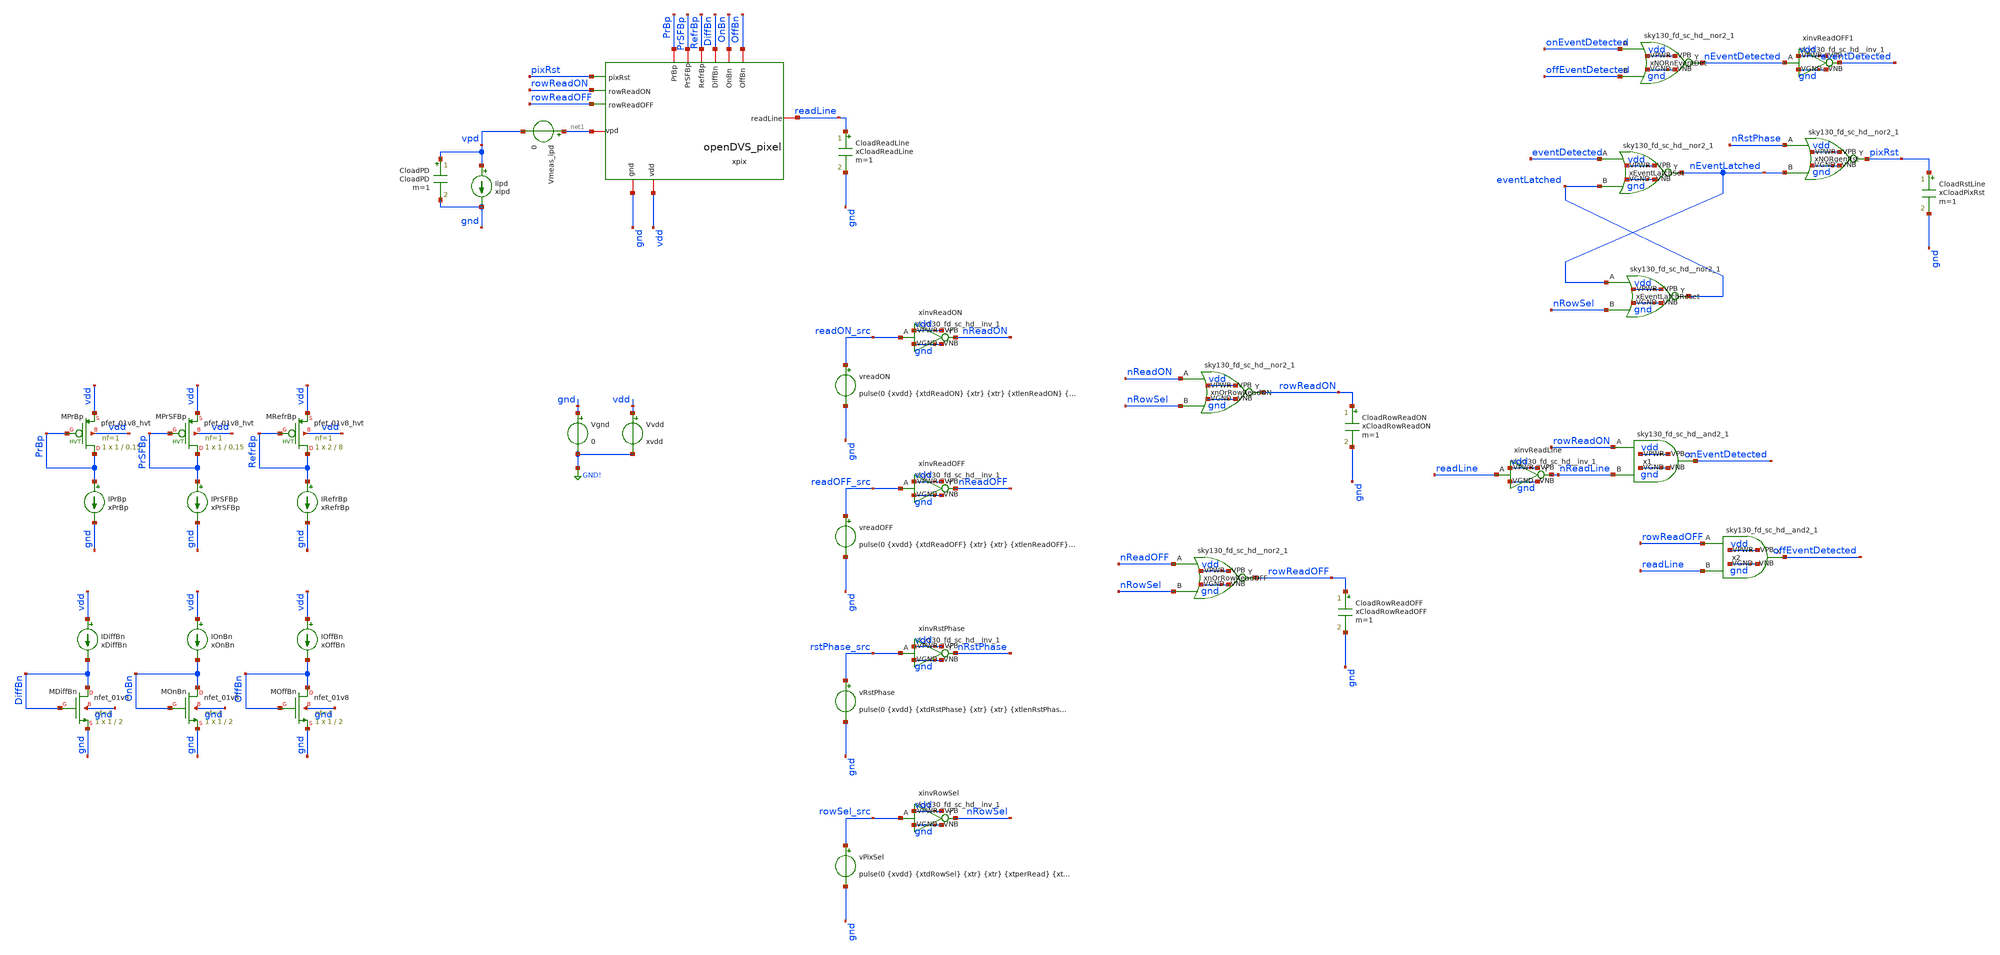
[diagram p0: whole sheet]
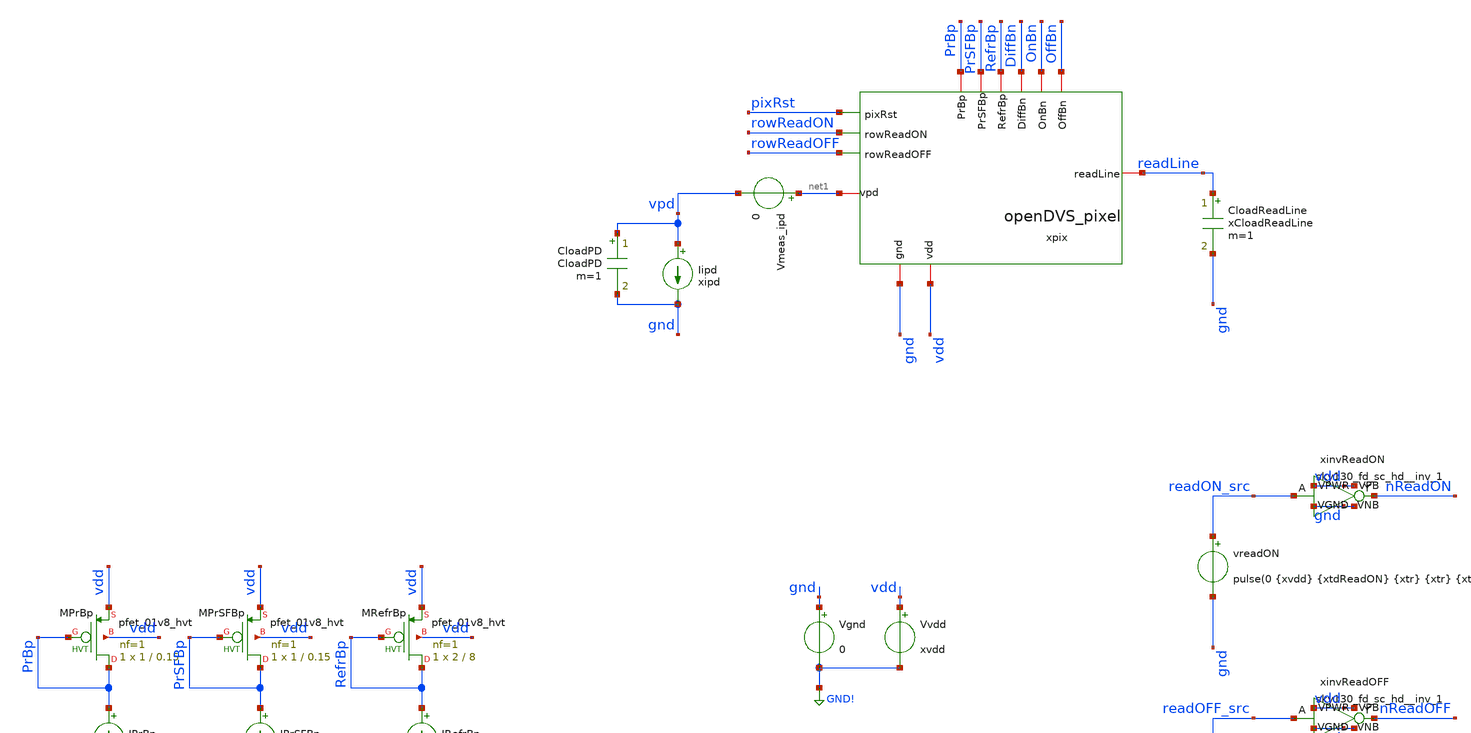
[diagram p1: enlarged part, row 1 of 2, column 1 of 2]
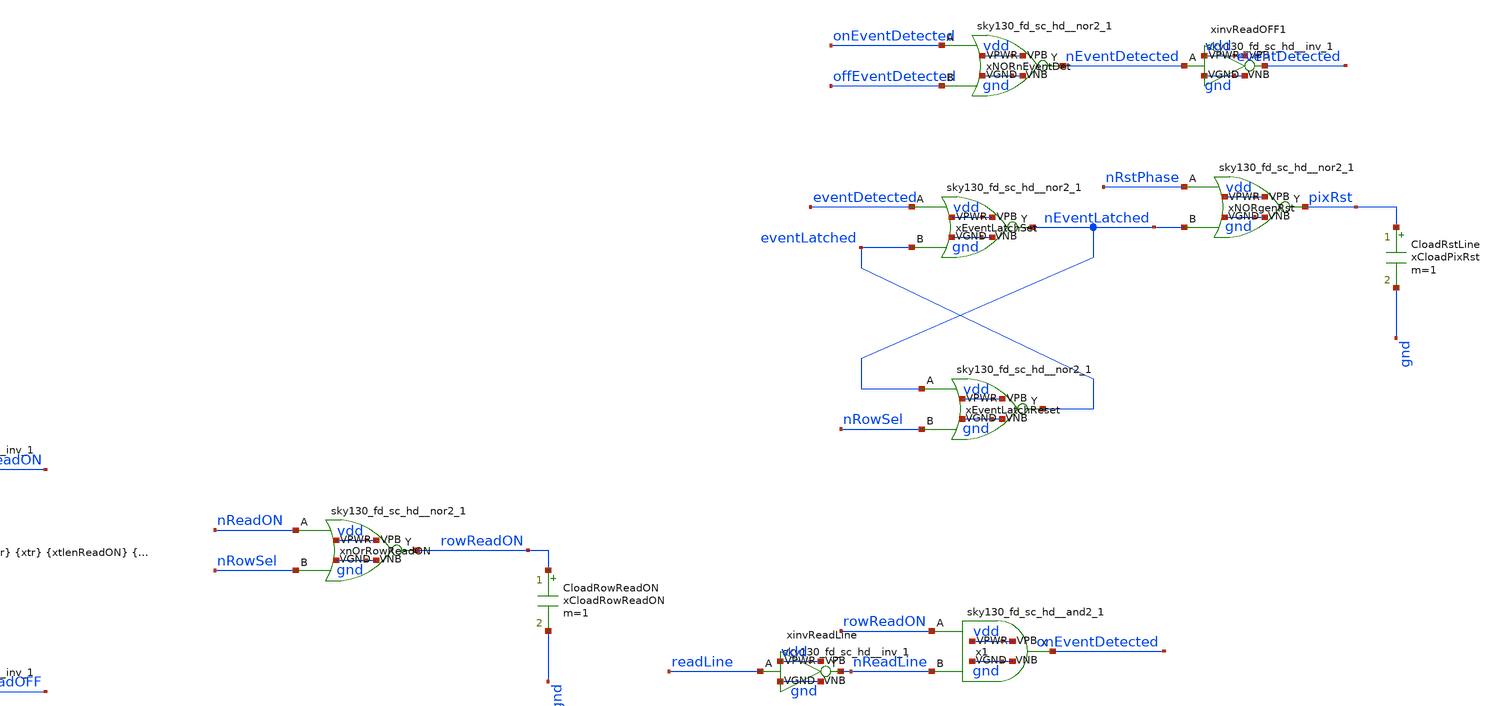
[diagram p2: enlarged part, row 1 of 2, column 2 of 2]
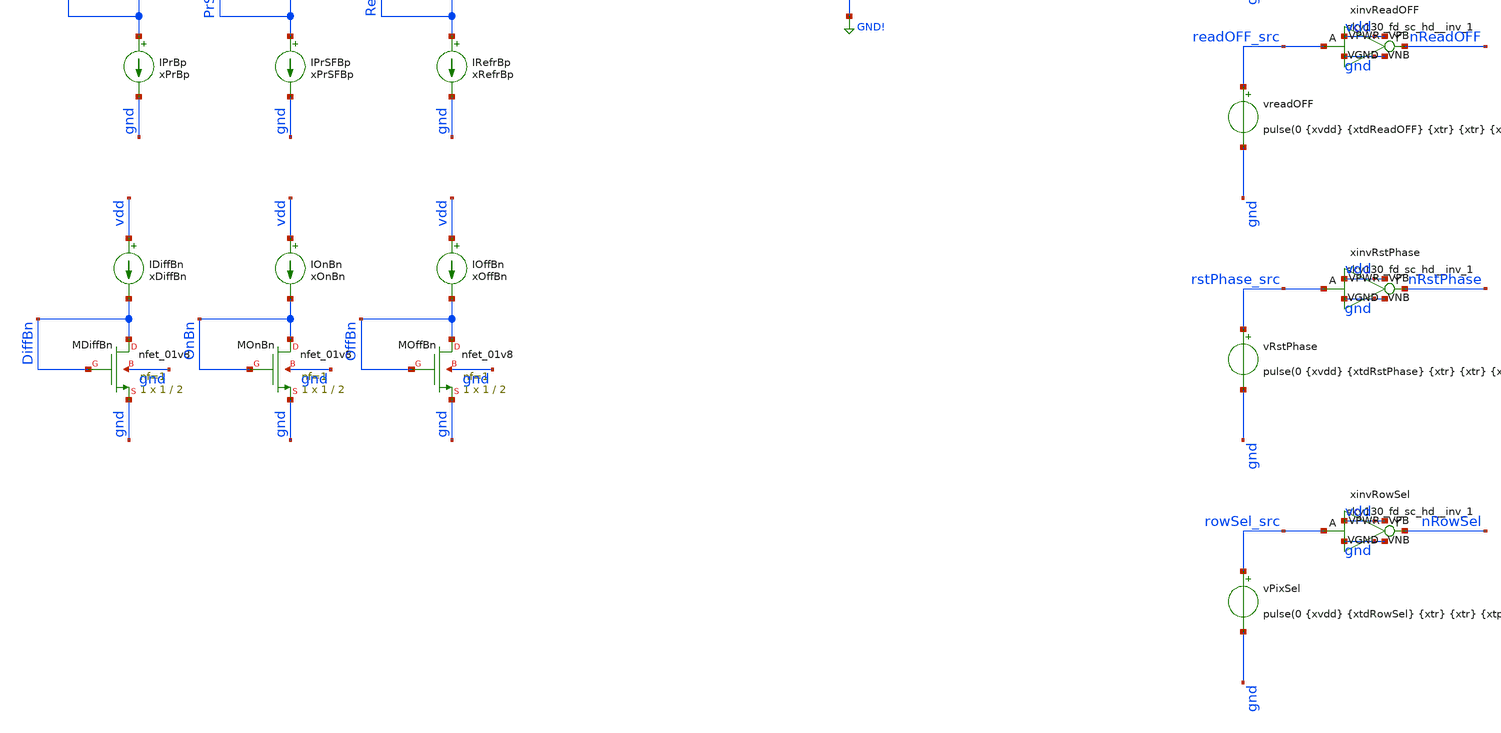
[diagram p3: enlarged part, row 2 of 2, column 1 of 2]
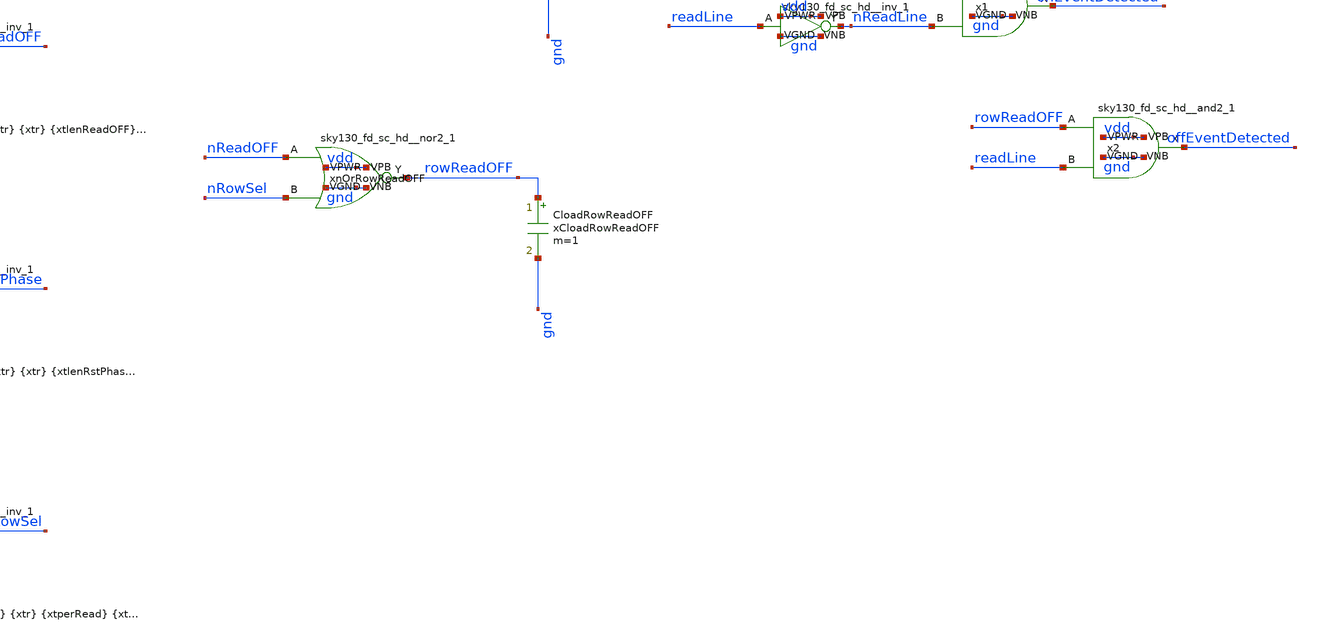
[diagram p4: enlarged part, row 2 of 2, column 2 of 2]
** sch_path: analog/xschem/pixel_tb.sch
**.subckt pixel_tb
xpix rowReadON vdd PrBp gnd net1 rowReadOFF pixRst PrSFBp DiffBn OnBn OffBn RefrBp readLine
+ openDVS_pixel
Vgnd gnd GND! 0
Vvdd vdd GND! xvdd
Iipd vpd gnd xipd
IRefrBp RefrBp gnd xRefrBp
XMRefrBp RefrBp RefrBp vdd vdd sky130_fd_pr__pfet_01v8_hvt L=8 W=2 nf=1 ad='int((1 + 1)/2) * 2 / 1 * 0.29'
+ as='int((1 + 2)/2) * 2 / 1 * 0.29' pd='2*int((1 + 1)/2) * (2 / 1 + 0.29)' ps='2*int((1 + 2)/2) * (2 / 1 + 0.29)'
+ nrd='0.29 / 2 ' nrs='0.29 / 2 ' sa=0 sb=0 sd=0 mult=1 m=1
IPrBp PrBp gnd xPrBp
XMPrBp PrBp PrBp vdd vdd sky130_fd_pr__pfet_01v8_hvt L=0.15 W=1 nf=1 ad='int((1 + 1)/2) * 1 / 1 * 0.29'
+ as='int((1 + 2)/2) * 1 / 1 * 0.29' pd='2*int((1 + 1)/2) * (1 / 1 + 0.29)' ps='2*int((1 + 2)/2) * (1 / 1 + 0.29)'
+ nrd='0.29 / 1 ' nrs='0.29 / 1 ' sa=0 sb=0 sd=0 mult=1 m=1
IPrSFBp PrSFBp gnd xPrSFBp
XMPrSFBp PrSFBp PrSFBp vdd vdd sky130_fd_pr__pfet_01v8_hvt L=0.15 W=1 nf=1 ad='int((1 + 1)/2) * 1 / 1 * 0.29'
+ as='int((1 + 2)/2) * 1 / 1 * 0.29' pd='2*int((1 + 1)/2) * (1 / 1 + 0.29)' ps='2*int((1 + 2)/2) * (1 / 1 + 0.29)'
+ nrd='0.29 / 1 ' nrs='0.29 / 1 ' sa=0 sb=0 sd=0 mult=1 m=1
XMDiffBn DiffBn DiffBn gnd gnd sky130_fd_pr__nfet_01v8 L=2 W=1 nf=1 ad='int((1 + 1)/2) * 1 / 1 * 0.29'
+ as='int((1 + 2)/2) * 1 / 1 * 0.29' pd='2*int((1 + 1)/2) * (1 / 1 + 0.29)' ps='2*int((1 + 2)/2) * (1 / 1 + 0.29)'
+ nrd='0.29 / 1 ' nrs='0.29 / 1 ' sa=0 sb=0 sd=0 mult=1 m=1
IDiffBn vdd DiffBn xDiffBn
XMOnBn OnBn OnBn gnd gnd sky130_fd_pr__nfet_01v8 L=2 W=1 nf=1 ad='int((1 + 1)/2) * 1 / 1 * 0.29' as='int((1 + 2)/2) * 1 / 1 * 0.29'
+ pd='2*int((1 + 1)/2) * (1 / 1 + 0.29)' ps='2*int((1 + 2)/2) * (1 / 1 + 0.29)' nrd='0.29 / 1 ' nrs='0.29 / 1 '
+ sa=0 sb=0 sd=0 mult=1 m=1
IOnBn vdd OnBn xOnBn
XMOffBn OffBn OffBn gnd gnd sky130_fd_pr__nfet_01v8 L=2 W=1 nf=1 ad='int((1 + 1)/2) * 1 / 1 * 0.29' as='int((1 + 2)/2) * 1 / 1 * 0.29'
+ pd='2*int((1 + 1)/2) * (1 / 1 + 0.29)' ps='2*int((1 + 2)/2) * (1 / 1 + 0.29)' nrd='0.29 / 1 ' nrs='0.29 / 1 '
+ sa=0 sb=0 sd=0 mult=1 m=1
IOffBn vdd OffBn xOffBn
vreadON readON_src gnd pulse(0 {xvdd} {xtdReadON} {xtr} {xtr} {xtlenReadON} {xtperRead})
CloadRowReadOFF rowReadOFF gnd xCloadRowReadOFF m=1
vreadOFF readOFF_src gnd pulse(0 {xvdd} {xtdReadOFF} {xtr} {xtr} {xtlenReadOFF} {xtperRead})
vPixSel rowSel_src gnd pulse(0 {xvdd} {xtdRowSel} {xtr} {xtr} {xtperRead} {xtperRowSel})
CloadReadLine readLine gnd xCloadReadLine m=1
xinvReadON readON_src nReadON vdd vdd gnd gnd sky130_fd_sc_hd__inv_1
xinvReadOFF readOFF_src nReadOFF vdd vdd gnd gnd sky130_fd_sc_hd__inv_1
xinvRowSel rowSel_src nRowSel vdd vdd gnd gnd sky130_fd_sc_hd__inv_1
xnOrRowReadOFF nReadOFF nRowSel rowReadOFF vdd vdd gnd gnd sky130_fd_sc_hd__nor2_1
CloadRowReadON rowReadON gnd xCloadRowReadON m=1
xnOrRowReadON nReadON nRowSel rowReadON vdd vdd gnd gnd sky130_fd_sc_hd__nor2_1
x1 rowReadON nReadLine vdd vdd gnd gnd onEventDetected sky130_fd_sc_hd__and2_1
xinvReadLine readLine nReadLine vdd vdd gnd gnd sky130_fd_sc_hd__inv_1
x2 rowReadOFF readLine vdd vdd gnd gnd offEventDetected sky130_fd_sc_hd__and2_1
xNORnEventDet onEventDetected offEventDetected nEventDetected vdd vdd gnd gnd
+ sky130_fd_sc_hd__nor2_1
xinvReadOFF1 nEventDetected eventDetected vdd vdd gnd gnd sky130_fd_sc_hd__inv_1
xEventLatchSet eventDetected eventLatched nEventLatched vdd vdd gnd gnd sky130_fd_sc_hd__nor2_1
xEventLatchReset nEventLatched nRowSel eventLatched vdd vdd gnd gnd sky130_fd_sc_hd__nor2_1
vRstPhase rstPhase_src gnd pulse(0 {xvdd} {xtdRstPhase} {xtr} {xtr} {xtlenRstPhase} {xtperRowSel})
xinvRstPhase rstPhase_src nRstPhase vdd vdd gnd gnd sky130_fd_sc_hd__inv_1
xNORgenRst nRstPhase nEventLatched pixRst vdd vdd gnd gnd sky130_fd_sc_hd__nor2_1
CloadRstLine pixRst gnd xCloadPixRst m=1
CloadPD vpd gnd CloadPD m=1
Vmeas_ipd net1 vpd 0
**** begin user architecture code

** opencircuitdesign pdks install
.lib $::SKYWATER_MODELS/sky130.lib.spice tt




.param xvdd = 1.8
.param xipd = 1e-9
.param xPrBp = 10n
.param xPrSFBp = 1n
.param xRefrBp = 4u
.param xDiffBn = 10n
.param xOnBn = 100n
.param xOffBn = 1n

.param xtr = 0.1n
.param xtperRead = 3u
.param xtdReadON = 100n
.param xtlenReadON = 950n
.param xtlenReadOFF = 950n
.param xtlenRstPhase = 950n
.param xtdReadOFF = 'xtdReadON+xtlenReadON+10n'
.param xtdRstPhase = 'xtdReadOFF+xtlenReadOFF+10n'
.param xtdRowSel = 50n
.param xtperRowSel = '2*xtperRead'

.param CloadPD = 30f
.param xCloadReadLine = 300f
.param xCloadRowReadON = 300f
.param xCloadRowReadOFF = 300f
.param xCloadPixRst = 300f

*Small Iphoto testing
Iphoto1 vpd gnd pulse(50n 100n 12u 5n 5n 5.99u 30u)
Iphoto2 vpd gnd pulse(50n 25n 24u 5n 5n 5.99u 30u)

.option gmin=1e-18 abstol=1e-15 vntol=1e-9 reltol=1e-6 chgtol=1e-16 trtol=6

.control

	save all
	op
	tran 0.1n 39u
        write pixel_tb.raw
.endc


**** end user architecture code
**.ends
.GLOBAL GND!
.end
